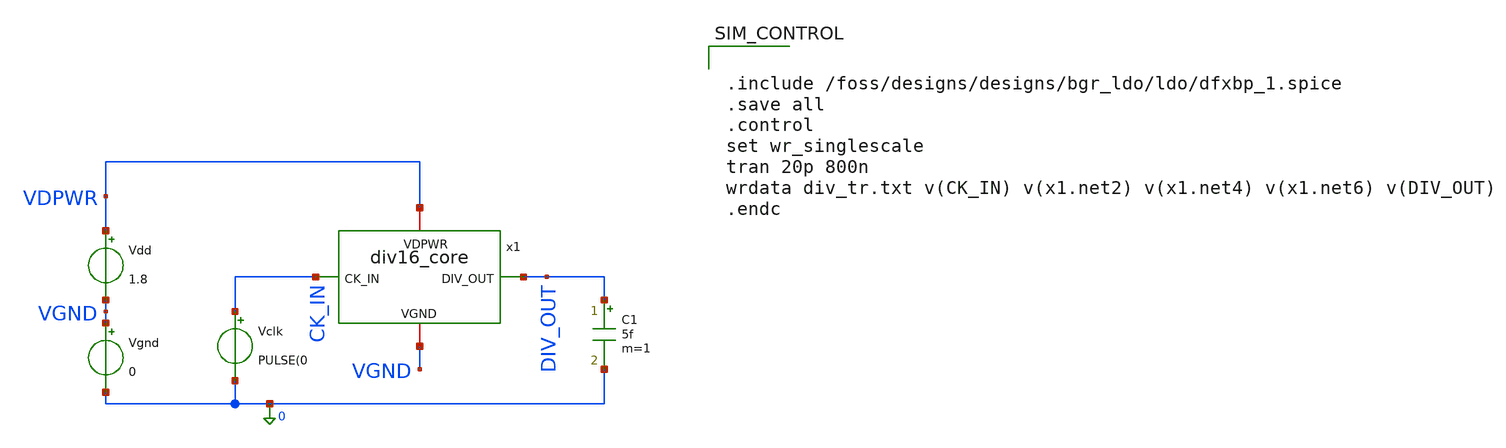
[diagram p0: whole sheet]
** sch_path: designs/bgr_ldo/ldo/div16_tb.sch
**.subckt div16_tb
x1 VDPWR VGND DIV_OUT CK_IN div16_core
Vclk CK_IN 0 PULSE(0
C1 DIV_OUT 0 5f m=1
Vdd VDPWR VGND 1.8
Vgnd VGND 0 0
**** begin user architecture code

** opencircuitdesign pdks install
.lib $::SKYWATER_MODELS/sky130.lib.spice tt



.include /foss/designs/designs/bgr_ldo/ldo/dfxbp_1.spice
.save all
.control
set wr_singlescale
tran 20p 800n
wrdata div_tr.txt v(CK_IN) v(x1.net2) v(x1.net4) v(x1.net6) v(DIV_OUT)
.endc



**** end user architecture code
**.ends

* expanding   symbol:  div16_core.sym # of pins=4
** sym_path: designs/bgr_ldo/ldo/div16_core.sym
** sch_path: designs/bgr_ldo/ldo/div16_core.sch
.subckt div16_core VDPWR VGND DIV_OUT CK_IN
*.ipin CK_IN
*.opin DIV_OUT
*.iopin VDPWR
*.iopin VGND
x1 CK_IN net1 VGND VGND VDPWR VDPWR net2 net1 sky130_fd_sc_hd__dfxbp_1
x2 net2 net3 VGND VGND VDPWR VDPWR net4 net3 sky130_fd_sc_hd__dfxbp_1
x3 net4 net5 VGND VGND VDPWR VDPWR net6 net5 sky130_fd_sc_hd__dfxbp_1
x4 net6 net7 VGND VGND VDPWR VDPWR DIV_OUT net7 sky130_fd_sc_hd__dfxbp_1
.ends

.end
